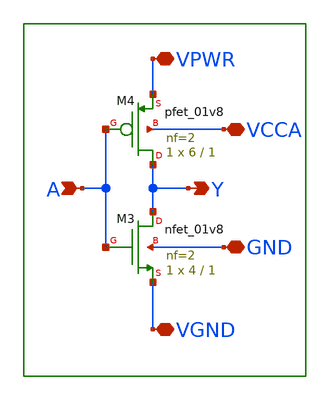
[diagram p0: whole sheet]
** sch_path: xschem/lib_dco/dco_main_inv.sch
**.subckt dco_main_inv VPWR VGND A Y VCCA GND
*.iopin VPWR
*.iopin VGND
*.ipin A
*.opin Y
*.iopin VCCA
*.iopin GND
XM3 Y A VGND GND sky130_fd_pr__nfet_01v8 L=1 W=4 nf=2 ad='int((nf+1)/2) * W/nf * 0.29' as='int((nf+2)/2) * W/nf * 0.29'
+ pd='2*int((nf+1)/2) * (W/nf + 0.29)' ps='2*int((nf+2)/2) * (W/nf + 0.29)' nrd='0.29 / W' nrs='0.29 / W'
+ sa=0 sb=0 sd=0 mult=1 m=1
XM4 Y A VPWR VCCA sky130_fd_pr__pfet_01v8 L=1 W=6 nf=2 ad='int((nf+1)/2) * W/nf * 0.29' as='int((nf+2)/2) * W/nf * 0.29'
+ pd='2*int((nf+1)/2) * (W/nf + 0.29)' ps='2*int((nf+2)/2) * (W/nf + 0.29)' nrd='0.29 / W' nrs='0.29 / W'
+ sa=0 sb=0 sd=0 mult=1 m=1
**.ends
.end
